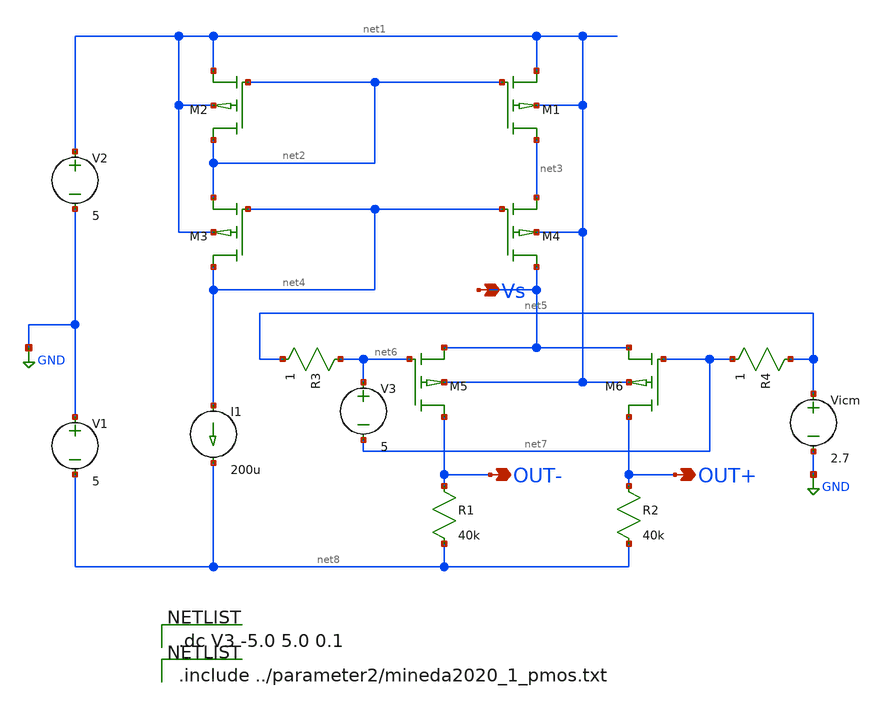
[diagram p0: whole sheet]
** sch_path: diffamp_test10umrealCS-Vcm-gain.sch
**.subckt diffamp_test10umrealCS-Vcm-gain Vs OUT+ OUT-
*.opin Vs
*.opin OUT+
*.opin OUT-
V1 GND net8 5
M1 net3 net2 net1 net1 YSS_PMOS w=14u l=14u as=0 ps=0 ad=0 pd=0 m=20
V2 net1 GND 5
I1 net4 net8 200u
M2 net2 net2 net1 net1 YSS_PMOS w=14u l=14u as=0 ps=0 ad=0 pd=0 m=20
V3 net6 net7 5
M3 net4 net4 net2 net1 YSS_PMOS w=14u l=14u as=0 ps=0 ad=0 pd=0 m=20
M4 Vs net4 net3 net1 YSS_PMOS w=14u l=14u as=0 ps=0 ad=0 pd=0 m=20
M5 OUT- net6 Vs net1 YSS_PMOS w=10u l=10u as=0 ps=0 ad=0 pd=0 m=10
M6 OUT+ net7 Vs net1 YSS_PMOS w=10u l=10u as=0 ps=0 ad=0 pd=0 m=10
R1 OUT- net8 40k m=1
R2 OUT+ net8 40k m=1
R3 net6 net5 1 m=1
R4 net5 net7 1 m=1
Vicm net5 GND 2.7
**** begin user architecture code

.dc V3 -5.0 5.0 0.1


.include ../parameter2/mineda2020_1_pmos.txt

**** end user architecture code
**.ends
.GLOBAL GND
.end
